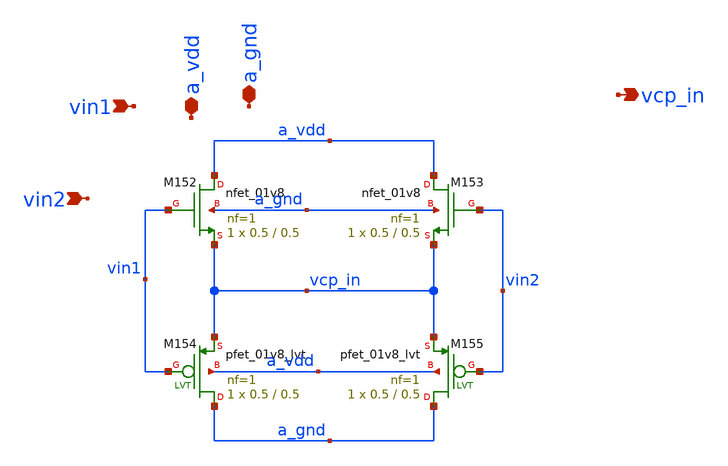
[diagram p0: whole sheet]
** sch_path: xschem/charge_pumps2/source_follower_buffer.sch
**.subckt source_follower_buffer vin1 a_vdd a_gnd vin2 vcp_in
*.ipin vin1
*.iopin a_vdd
*.iopin a_gnd
*.ipin vin2
*.opin vcp_in
XM152 a_vdd vin1 vcp_in a_gnd sky130_fd_pr__nfet_01v8 L=0.5 W=0.5 nf=1 ad='int((nf+1)/2) * W/nf * 0.29'
+ as='int((nf+2)/2) * W/nf * 0.29' pd='2*int((nf+1)/2) * (W/nf + 0.29)' ps='2*int((nf+2)/2) * (W/nf + 0.29)'
+ nrd='0.29 / W' nrs='0.29 / W' sa=0 sb=0 sd=0 mult=1 m=1
XM153 a_vdd vin2 vcp_in a_gnd sky130_fd_pr__nfet_01v8 L=0.5 W=0.5 nf=1 ad='int((nf+1)/2) * W/nf * 0.29'
+ as='int((nf+2)/2) * W/nf * 0.29' pd='2*int((nf+1)/2) * (W/nf + 0.29)' ps='2*int((nf+2)/2) * (W/nf + 0.29)'
+ nrd='0.29 / W' nrs='0.29 / W' sa=0 sb=0 sd=0 mult=1 m=1
XM154 a_gnd vin1 vcp_in a_vdd sky130_fd_pr__pfet_01v8_lvt L=0.5 W=0.5 nf=1 ad='int((nf+1)/2) * W/nf * 0.29'
+ as='int((nf+2)/2) * W/nf * 0.29' pd='2*int((nf+1)/2) * (W/nf + 0.29)' ps='2*int((nf+2)/2) * (W/nf + 0.29)'
+ nrd='0.29 / W' nrs='0.29 / W' sa=0 sb=0 sd=0 mult=1 m=1
XM155 a_gnd vin2 vcp_in a_vdd sky130_fd_pr__pfet_01v8_lvt L=0.5 W=0.5 nf=1 ad='int((nf+1)/2) * W/nf * 0.29'
+ as='int((nf+2)/2) * W/nf * 0.29' pd='2*int((nf+1)/2) * (W/nf + 0.29)' ps='2*int((nf+2)/2) * (W/nf + 0.29)'
+ nrd='0.29 / W' nrs='0.29 / W' sa=0 sb=0 sd=0 mult=1 m=1
**.ends
.end
